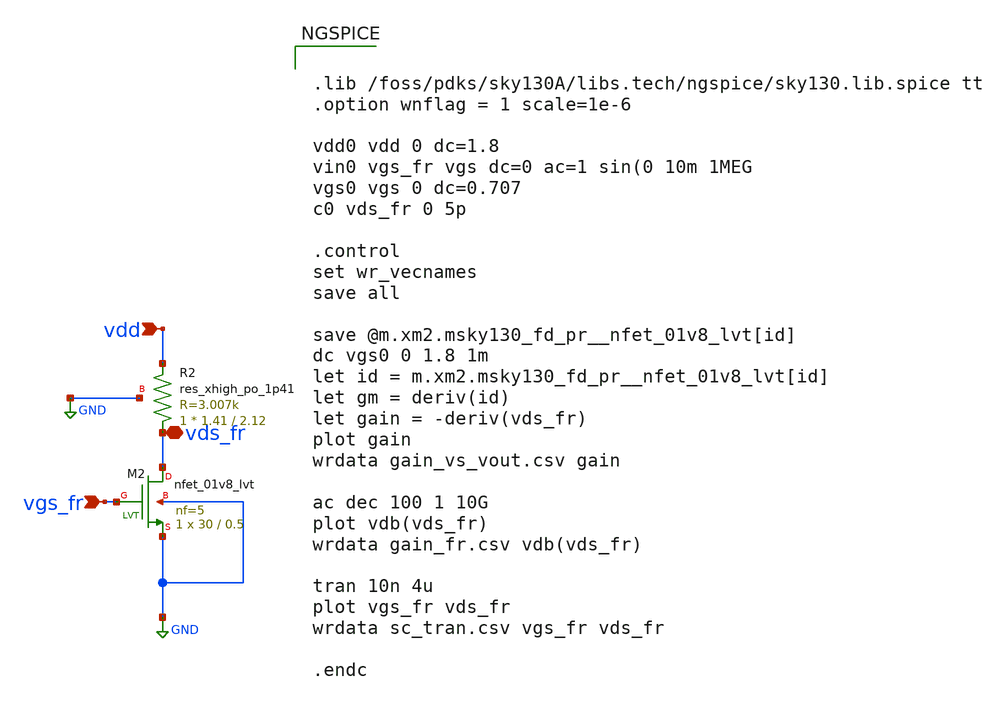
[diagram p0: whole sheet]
** sch_path: cs_amp/schematic/cs.sch
**.subckt cs vds_fr vdd vgs_fr
*.iopin vds_fr
*.ipin vdd
*.ipin vgs_fr
XM2 vds_fr vgs_fr GND GND sky130_fd_pr__nfet_01v8_lvt L=0.5 W=30 nf=5 ad='int((nf+1)/2) * W/nf * 0.29'
+ as='int((nf+2)/2) * W/nf * 0.29' pd='2*int((nf+1)/2) * (W/nf + 0.29)' ps='2*int((nf+2)/2) * (W/nf + 0.29)'
+ nrd='0.29 / W' nrs='0.29 / W' sa=0 sb=0 sd=0 mult=1 m=1
XR2 vds_fr vdd GND sky130_fd_pr__res_xhigh_po_1p41 L=2.12 mult=1 m=1
**** begin user architecture code


.lib /foss/pdks/sky130A/libs.tech/ngspice/sky130.lib.spice tt
.option wnflag = 1 scale=1e-6

vdd0 vdd 0 dc=1.8
vin0 vgs_fr vgs dc=0 ac=1 sin(0 10m 1MEG
vgs0 vgs 0 dc=0.707
c0 vds_fr 0 5p

.control
set wr_vecnames
save all

save @m.xm2.msky130_fd_pr__nfet_01v8_lvt[id]
dc vgs0 0 1.8 1m
let id = m.xm2.msky130_fd_pr__nfet_01v8_lvt[id]
let gm = deriv(id)
let gain = -deriv(vds_fr)
plot gain
wrdata gain_vs_vout.csv gain

ac dec 100 1 10G
plot vdb(vds_fr)
wrdata gain_fr.csv vdb(vds_fr)

tran 10n 4u
plot vgs_fr vds_fr
wrdata sc_tran.csv vgs_fr vds_fr

.endc


**** end user architecture code
**.ends
.GLOBAL GND
.end
